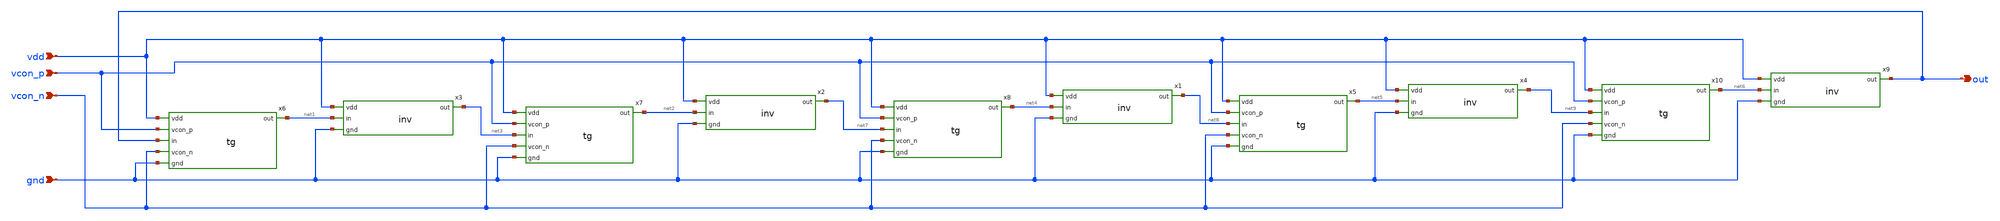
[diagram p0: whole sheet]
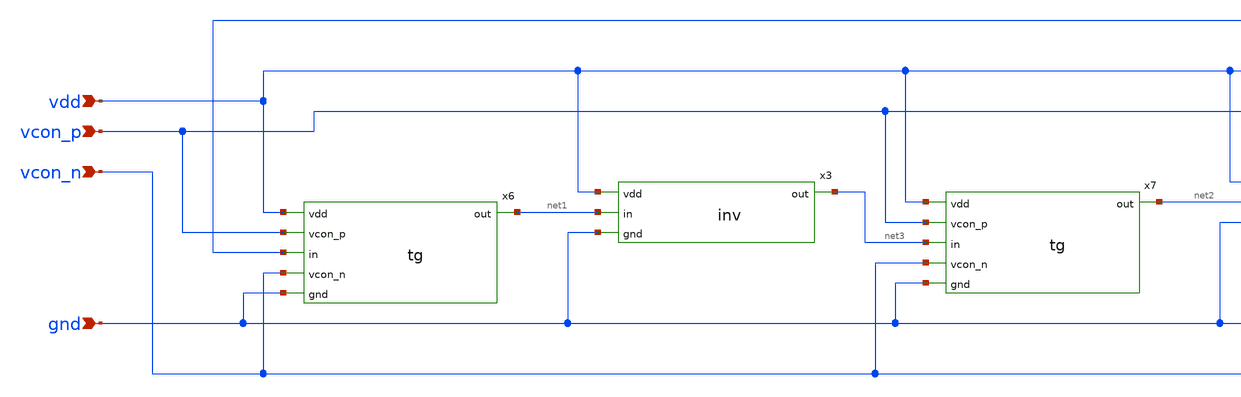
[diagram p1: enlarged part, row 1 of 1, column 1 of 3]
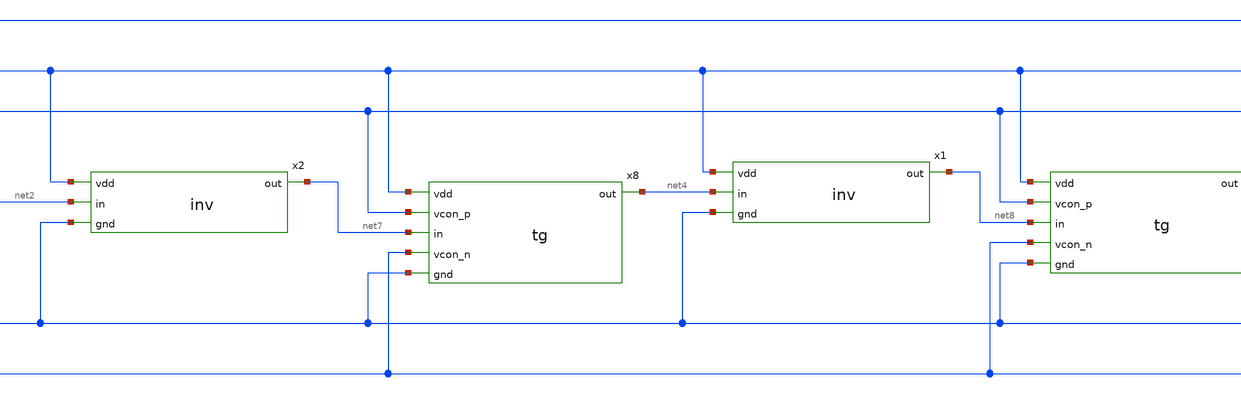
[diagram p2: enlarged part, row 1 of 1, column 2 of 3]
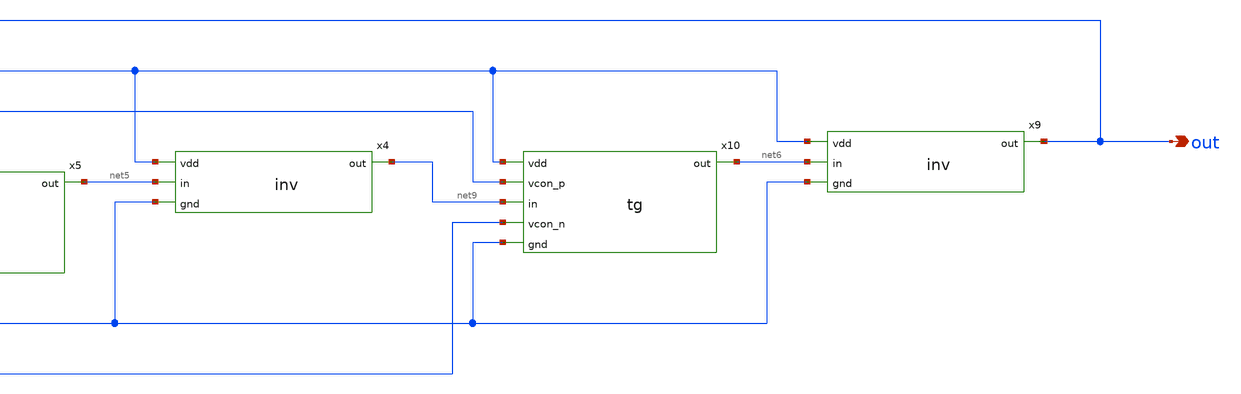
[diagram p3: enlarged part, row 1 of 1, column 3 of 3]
** sch_path: xschem/vcro_5st.sch
**.subckt vcro_5st vdd vcon_p vcon_n gnd out
*.ipin vdd
*.ipin vcon_p
*.ipin vcon_n
*.ipin gnd
*.opin out
x1 vdd net4 net8 gnd inv
x2 vdd net2 net7 gnd inv
x3 vdd net1 net3 gnd inv
x6 vdd vcon_p net1 out vcon_n gnd tg
x7 vdd vcon_p net2 net3 vcon_n gnd tg
x8 vdd vcon_p net4 net7 vcon_n gnd tg
x4 vdd net5 net9 gnd inv
x5 vdd vcon_p net5 net8 vcon_n gnd tg
x9 vdd net6 out gnd inv
x10 vdd vcon_p net6 net9 vcon_n gnd tg
**.ends
.end
